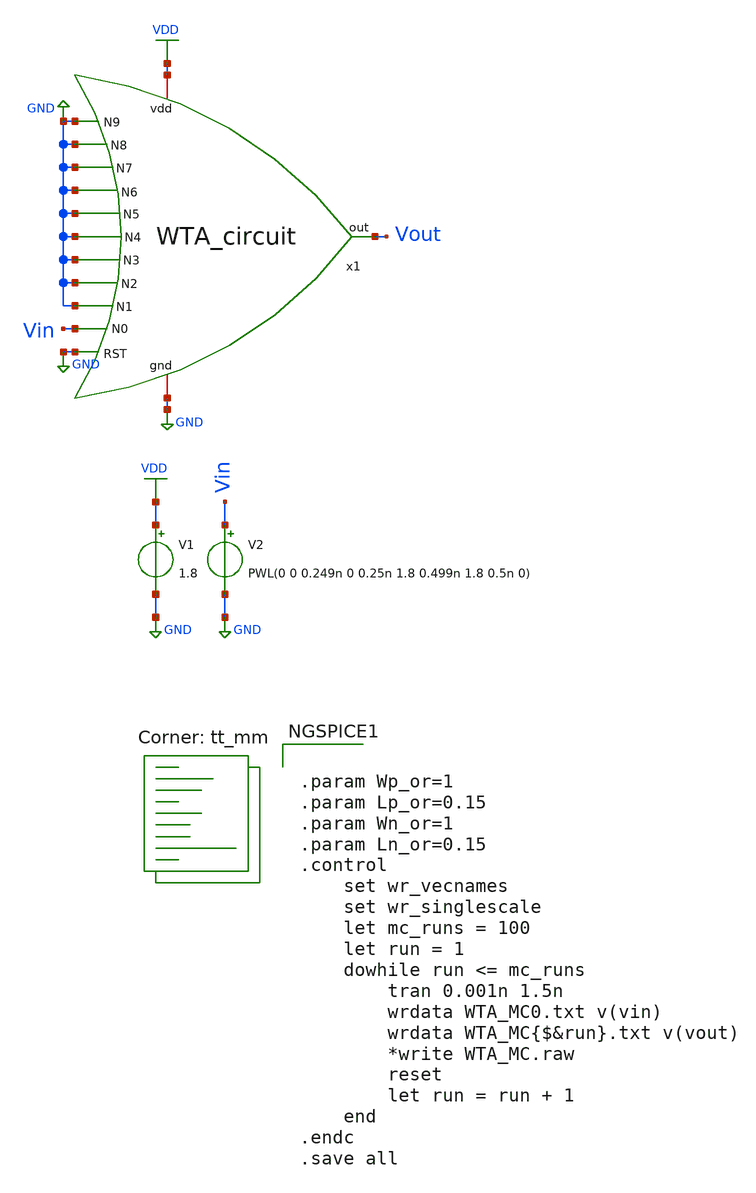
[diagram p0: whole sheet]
** sch_path: Final_Design/WTA_MC_tb.sch
**.subckt WTA_MC_tb
V1 VDD GND 1.8
V2 Vin GND PWL(0 0 0.249n 0 0.25n 1.8 0.499n 1.8 0.5n 0)
x1 VDD GND GND GND GND GND GND GND GND GND GND Vin Vout GND WTA_circuit
**** begin user architecture code
.lib $::SKYWATER_MODELS/sky130.lib.spice tt_mm


.param Wp_or=1
.param Lp_or=0.15
.param Wn_or=1
.param Ln_or=0.15
.control
	set wr_vecnames
	set wr_singlescale
	let mc_runs = 100
	let run = 1
	dowhile run <= mc_runs
		tran 0.001n 1.5n
		wrdata WTA_MC0.txt v(vin)
		wrdata WTA_MC{$&run}.txt v(vout)
		*write WTA_MC.raw
		reset
		let run = run + 1
	end
.endc
.save all


**** end user architecture code
**.ends

* expanding   symbol:  /home/ricardo/RATT_repos/Proyectos_xschem/SNN/WTA_circuit.sym # of pins=14
** sym_path: Final_Design/WTA_circuit.sym
** sch_path: Final_Design/WTA_circuit.sch
.subckt WTA_circuit vdd RST N9 N8 N7 N6 N5 N4 N3 N2 N1 N0 out gnd
*.iopin gnd
*.ipin N0
*.ipin N1
*.opin out
*.iopin vdd
*.ipin N2
*.ipin N3
*.ipin N4
*.ipin N5
*.ipin N6
*.ipin N7
*.ipin N8
*.ipin N9
*.ipin RST
XM2 out net3 gnd gnd sky130_fd_pr__nfet_01v8 L=0.15 W=1.5 nf=1 ad='int((nf+1)/2) * W/nf * 0.29' as='int((nf+2)/2) * W/nf * 0.29'
+ pd='2*int((nf+1)/2) * (W/nf + 0.29)' ps='2*int((nf+2)/2) * (W/nf + 0.29)' nrd='0.29 / W' nrs='0.29 / W'
+ sa=0 sb=0 sd=0 mult=1 m=1
XM1 out net3 vdd vdd sky130_fd_pr__pfet_01v8 L=0.15 W=1.5 nf=1 ad='int((nf+1)/2) * W/nf * 0.29' as='int((nf+2)/2) * W/nf * 0.29'
+ pd='2*int((nf+1)/2) * (W/nf + 0.29)' ps='2*int((nf+2)/2) * (W/nf + 0.29)' nrd='0.29 / W' nrs='0.29 / W'
+ sa=0 sb=0 sd=0 mult=1 m=1
XM19 net9 N8 net10 vdd sky130_fd_pr__pfet_01v8 L=0.15 W=1.5 nf=1 ad='int((nf+1)/2) * W/nf * 0.29' as='int((nf+2)/2) * W/nf * 0.29'
+ pd='2*int((nf+1)/2) * (W/nf + 0.29)' ps='2*int((nf+2)/2) * (W/nf + 0.29)' nrd='0.29 / W' nrs='0.29 / W'
+ sa=0 sb=0 sd=0 mult=1 m=1
XM21 net10 N9 net11 vdd sky130_fd_pr__pfet_01v8 L=0.15 W=1.5 nf=1 ad='int((nf+1)/2) * W/nf * 0.29' as='int((nf+2)/2) * W/nf * 0.29'
+ pd='2*int((nf+1)/2) * (W/nf + 0.29)' ps='2*int((nf+2)/2) * (W/nf + 0.29)' nrd='0.29 / W' nrs='0.29 / W'
+ sa=0 sb=0 sd=0 mult=1 m=1
XM23 net11 RST vdd vdd sky130_fd_pr__pfet_01v8 L=0.15 W=1.5 nf=1 ad='int((nf+1)/2) * W/nf * 0.29' as='int((nf+2)/2) * W/nf * 0.29'
+ pd='2*int((nf+1)/2) * (W/nf + 0.29)' ps='2*int((nf+2)/2) * (W/nf + 0.29)' nrd='0.29 / W' nrs='0.29 / W'
+ sa=0 sb=0 sd=0 mult=1 m=1
XM3 net3 N0 net1 vdd sky130_fd_pr__pfet_01v8 L=0.15 W=1.5 nf=1 ad='int((nf+1)/2) * W/nf * 0.29' as='int((nf+2)/2) * W/nf * 0.29'
+ pd='2*int((nf+1)/2) * (W/nf + 0.29)' ps='2*int((nf+2)/2) * (W/nf + 0.29)' nrd='0.29 / W' nrs='0.29 / W'
+ sa=0 sb=0 sd=0 mult=1 m=1
XM5 net1 N1 net2 vdd sky130_fd_pr__pfet_01v8 L=0.15 W=1.5 nf=1 ad='int((nf+1)/2) * W/nf * 0.29' as='int((nf+2)/2) * W/nf * 0.29'
+ pd='2*int((nf+1)/2) * (W/nf + 0.29)' ps='2*int((nf+2)/2) * (W/nf + 0.29)' nrd='0.29 / W' nrs='0.29 / W'
+ sa=0 sb=0 sd=0 mult=1 m=1
XM7 net2 N2 net4 vdd sky130_fd_pr__pfet_01v8 L=0.15 W=1.5 nf=1 ad='int((nf+1)/2) * W/nf * 0.29' as='int((nf+2)/2) * W/nf * 0.29'
+ pd='2*int((nf+1)/2) * (W/nf + 0.29)' ps='2*int((nf+2)/2) * (W/nf + 0.29)' nrd='0.29 / W' nrs='0.29 / W'
+ sa=0 sb=0 sd=0 mult=1 m=1
XM9 net4 N3 net5 vdd sky130_fd_pr__pfet_01v8 L=0.15 W=1.5 nf=1 ad='int((nf+1)/2) * W/nf * 0.29' as='int((nf+2)/2) * W/nf * 0.29'
+ pd='2*int((nf+1)/2) * (W/nf + 0.29)' ps='2*int((nf+2)/2) * (W/nf + 0.29)' nrd='0.29 / W' nrs='0.29 / W'
+ sa=0 sb=0 sd=0 mult=1 m=1
XM11 net5 N4 net6 vdd sky130_fd_pr__pfet_01v8 L=0.15 W=1.5 nf=1 ad='int((nf+1)/2) * W/nf * 0.29' as='int((nf+2)/2) * W/nf * 0.29'
+ pd='2*int((nf+1)/2) * (W/nf + 0.29)' ps='2*int((nf+2)/2) * (W/nf + 0.29)' nrd='0.29 / W' nrs='0.29 / W'
+ sa=0 sb=0 sd=0 mult=1 m=1
XM13 net6 N5 net7 vdd sky130_fd_pr__pfet_01v8 L=0.15 W=1.5 nf=1 ad='int((nf+1)/2) * W/nf * 0.29' as='int((nf+2)/2) * W/nf * 0.29'
+ pd='2*int((nf+1)/2) * (W/nf + 0.29)' ps='2*int((nf+2)/2) * (W/nf + 0.29)' nrd='0.29 / W' nrs='0.29 / W'
+ sa=0 sb=0 sd=0 mult=1 m=1
XM15 net7 N6 net8 vdd sky130_fd_pr__pfet_01v8 L=0.15 W=1.5 nf=1 ad='int((nf+1)/2) * W/nf * 0.29' as='int((nf+2)/2) * W/nf * 0.29'
+ pd='2*int((nf+1)/2) * (W/nf + 0.29)' ps='2*int((nf+2)/2) * (W/nf + 0.29)' nrd='0.29 / W' nrs='0.29 / W'
+ sa=0 sb=0 sd=0 mult=1 m=1
XM17 net8 N7 net9 vdd sky130_fd_pr__pfet_01v8 L=0.15 W=1.5 nf=1 ad='int((nf+1)/2) * W/nf * 0.29' as='int((nf+2)/2) * W/nf * 0.29'
+ pd='2*int((nf+1)/2) * (W/nf + 0.29)' ps='2*int((nf+2)/2) * (W/nf + 0.29)' nrd='0.29 / W' nrs='0.29 / W'
+ sa=0 sb=0 sd=0 mult=1 m=1
XM4 net3 N0 gnd gnd sky130_fd_pr__nfet_01v8 L=0.15 W=1.5 nf=1 ad='int((nf+1)/2) * W/nf * 0.29' as='int((nf+2)/2) * W/nf * 0.29'
+ pd='2*int((nf+1)/2) * (W/nf + 0.29)' ps='2*int((nf+2)/2) * (W/nf + 0.29)' nrd='0.29 / W' nrs='0.29 / W'
+ sa=0 sb=0 sd=0 mult=1 m=1
XM6 net3 N1 gnd gnd sky130_fd_pr__nfet_01v8 L=0.15 W=1.5 nf=1 ad='int((nf+1)/2) * W/nf * 0.29' as='int((nf+2)/2) * W/nf * 0.29'
+ pd='2*int((nf+1)/2) * (W/nf + 0.29)' ps='2*int((nf+2)/2) * (W/nf + 0.29)' nrd='0.29 / W' nrs='0.29 / W'
+ sa=0 sb=0 sd=0 mult=1 m=1
XM8 net3 N2 gnd gnd sky130_fd_pr__nfet_01v8 L=0.15 W=1.5 nf=1 ad='int((nf+1)/2) * W/nf * 0.29' as='int((nf+2)/2) * W/nf * 0.29'
+ pd='2*int((nf+1)/2) * (W/nf + 0.29)' ps='2*int((nf+2)/2) * (W/nf + 0.29)' nrd='0.29 / W' nrs='0.29 / W'
+ sa=0 sb=0 sd=0 mult=1 m=1
XM10 net3 N3 gnd gnd sky130_fd_pr__nfet_01v8 L=0.15 W=1.5 nf=1 ad='int((nf+1)/2) * W/nf * 0.29' as='int((nf+2)/2) * W/nf * 0.29'
+ pd='2*int((nf+1)/2) * (W/nf + 0.29)' ps='2*int((nf+2)/2) * (W/nf + 0.29)' nrd='0.29 / W' nrs='0.29 / W'
+ sa=0 sb=0 sd=0 mult=1 m=1
XM12 net3 N4 gnd gnd sky130_fd_pr__nfet_01v8 L=0.15 W=1.5 nf=1 ad='int((nf+1)/2) * W/nf * 0.29' as='int((nf+2)/2) * W/nf * 0.29'
+ pd='2*int((nf+1)/2) * (W/nf + 0.29)' ps='2*int((nf+2)/2) * (W/nf + 0.29)' nrd='0.29 / W' nrs='0.29 / W'
+ sa=0 sb=0 sd=0 mult=1 m=1
XM14 net3 N5 gnd gnd sky130_fd_pr__nfet_01v8 L=0.15 W=1.5 nf=1 ad='int((nf+1)/2) * W/nf * 0.29' as='int((nf+2)/2) * W/nf * 0.29'
+ pd='2*int((nf+1)/2) * (W/nf + 0.29)' ps='2*int((nf+2)/2) * (W/nf + 0.29)' nrd='0.29 / W' nrs='0.29 / W'
+ sa=0 sb=0 sd=0 mult=1 m=1
XM16 net3 N6 gnd gnd sky130_fd_pr__nfet_01v8 L=0.15 W=1.5 nf=1 ad='int((nf+1)/2) * W/nf * 0.29' as='int((nf+2)/2) * W/nf * 0.29'
+ pd='2*int((nf+1)/2) * (W/nf + 0.29)' ps='2*int((nf+2)/2) * (W/nf + 0.29)' nrd='0.29 / W' nrs='0.29 / W'
+ sa=0 sb=0 sd=0 mult=1 m=1
XM18 net3 N7 gnd gnd sky130_fd_pr__nfet_01v8 L=0.15 W=1.5 nf=1 ad='int((nf+1)/2) * W/nf * 0.29' as='int((nf+2)/2) * W/nf * 0.29'
+ pd='2*int((nf+1)/2) * (W/nf + 0.29)' ps='2*int((nf+2)/2) * (W/nf + 0.29)' nrd='0.29 / W' nrs='0.29 / W'
+ sa=0 sb=0 sd=0 mult=1 m=1
XM20 net3 N8 gnd gnd sky130_fd_pr__nfet_01v8 L=0.15 W=1.5 nf=1 ad='int((nf+1)/2) * W/nf * 0.29' as='int((nf+2)/2) * W/nf * 0.29'
+ pd='2*int((nf+1)/2) * (W/nf + 0.29)' ps='2*int((nf+2)/2) * (W/nf + 0.29)' nrd='0.29 / W' nrs='0.29 / W'
+ sa=0 sb=0 sd=0 mult=1 m=1
XM22 net3 N9 gnd gnd sky130_fd_pr__nfet_01v8 L=0.15 W=1.5 nf=1 ad='int((nf+1)/2) * W/nf * 0.29' as='int((nf+2)/2) * W/nf * 0.29'
+ pd='2*int((nf+1)/2) * (W/nf + 0.29)' ps='2*int((nf+2)/2) * (W/nf + 0.29)' nrd='0.29 / W' nrs='0.29 / W'
+ sa=0 sb=0 sd=0 mult=1 m=1
XM24 net3 RST gnd gnd sky130_fd_pr__nfet_01v8 L=0.15 W=1.5 nf=1 ad='int((nf+1)/2) * W/nf * 0.29' as='int((nf+2)/2) * W/nf * 0.29'
+ pd='2*int((nf+1)/2) * (W/nf + 0.29)' ps='2*int((nf+2)/2) * (W/nf + 0.29)' nrd='0.29 / W' nrs='0.29 / W'
+ sa=0 sb=0 sd=0 mult=1 m=1
.ends

.GLOBAL GND
.GLOBAL VDD
.end
